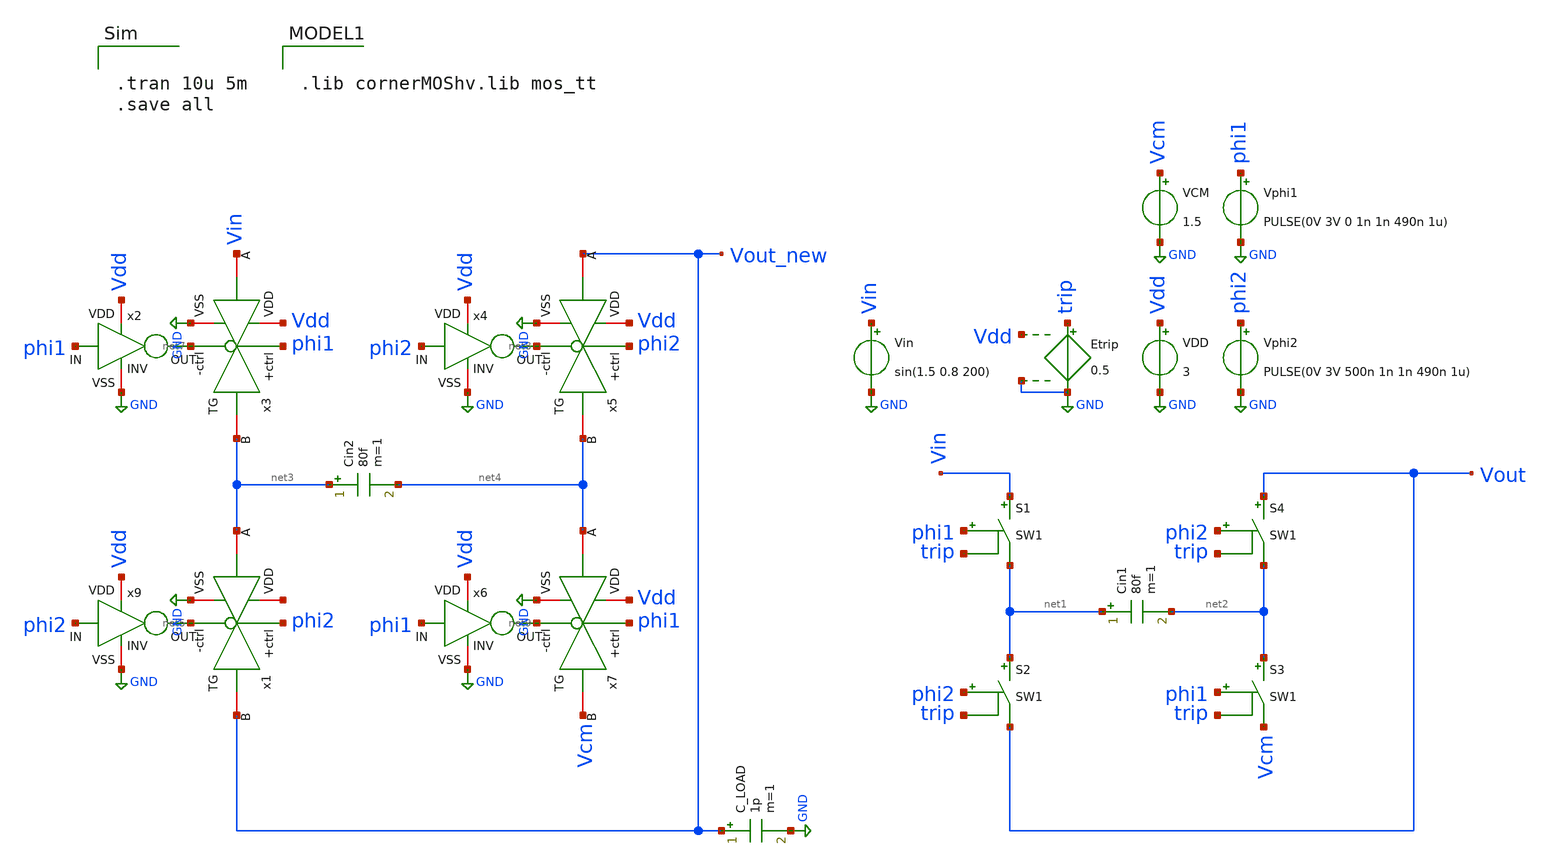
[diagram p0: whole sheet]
** sch_path: real_circuit/final/SW_tb.sch
**.subckt SW_tb
S2 net1 Vout phi2 trip SW1
S1 Vin net1 phi1 trip SW1
S3 net2 Vcm phi1 trip SW1
S4 Vout net2 phi2 trip SW1
Cin1 net1 net2 80f m=1
Etrip trip GND Vdd GND 0.5
VDD Vdd GND 3
VCM Vcm GND 1.5
Vin Vin GND sin(1.5 0.8 200)
Vphi1 phi1 GND PULSE(0V 3V 0 1n 1n 490n 1u)
Vphi2 phi2 GND PULSE(0V 3V 500n 1n 1n 490n 1u)
C_LOAD Vout_new GND 1p m=1
x9 Vdd phi2 net5 GND INV
x1 phi2 net6 Vout_new net3 net5 GND TG
x2 Vdd phi1 net7 GND INV
x3 phi1 Vdd net3 Vin net7 GND TG
x4 Vdd phi2 net8 GND INV
x5 phi2 Vdd net4 Vout_new net8 GND TG
x6 Vdd phi1 net9 GND INV
x7 phi1 Vdd Vcm net4 net9 GND TG
Cin2 net3 net4 80f m=1
**** begin user architecture code


.tran 10u 5m
.save all



.lib cornerMOShv.lib mos_tt

**** end user architecture code
**.ends

* expanding   symbol:  /foss/designs/final/INV.sym # of pins=4
** sym_path: real_circuit/final/INV.sym
** sch_path: real_circuit/final/INV.sch
.subckt INV VDD IN OUT VSS
*.iopin VDD
*.iopin VSS
*.ipin IN
*.opin OUT
XM1 OUT IN VDD VDD sg13_hv_pmos w=2u l=0.6u ng=1 m=1 mm_ok=1
XM2 OUT IN VSS VSS sg13_hv_nmos w=1u l=0.6u ng=1 m=1 mm_ok=1
.ends


* expanding   symbol:  /foss/designs/final/TG.sym # of pins=6
** sym_path: real_circuit/final/TG.sym
** sch_path: real_circuit/final/TG.sch
.subckt TG +ctrl VDD B A -ctrl VSS
*.iopin A
*.iopin B
*.iopin VDD
*.iopin VSS
*.ipin +ctrl
*.ipin -ctrl
XM1 B -ctrl A VSS sg13_hv_nmos w=1u l=0.6u ng=1 m=1 mm_ok=1
XM2 B +ctrl A VDD sg13_hv_pmos w=2.5u l=0.6u ng=1 m=1 mm_ok=1
.ends

.GLOBAL GND
**** begin user architecture code
.MODEL SW1 SW   VT=0.9 VH=0.01  RON=0.1 ROFF=10G
**** end user architecture code
.end
